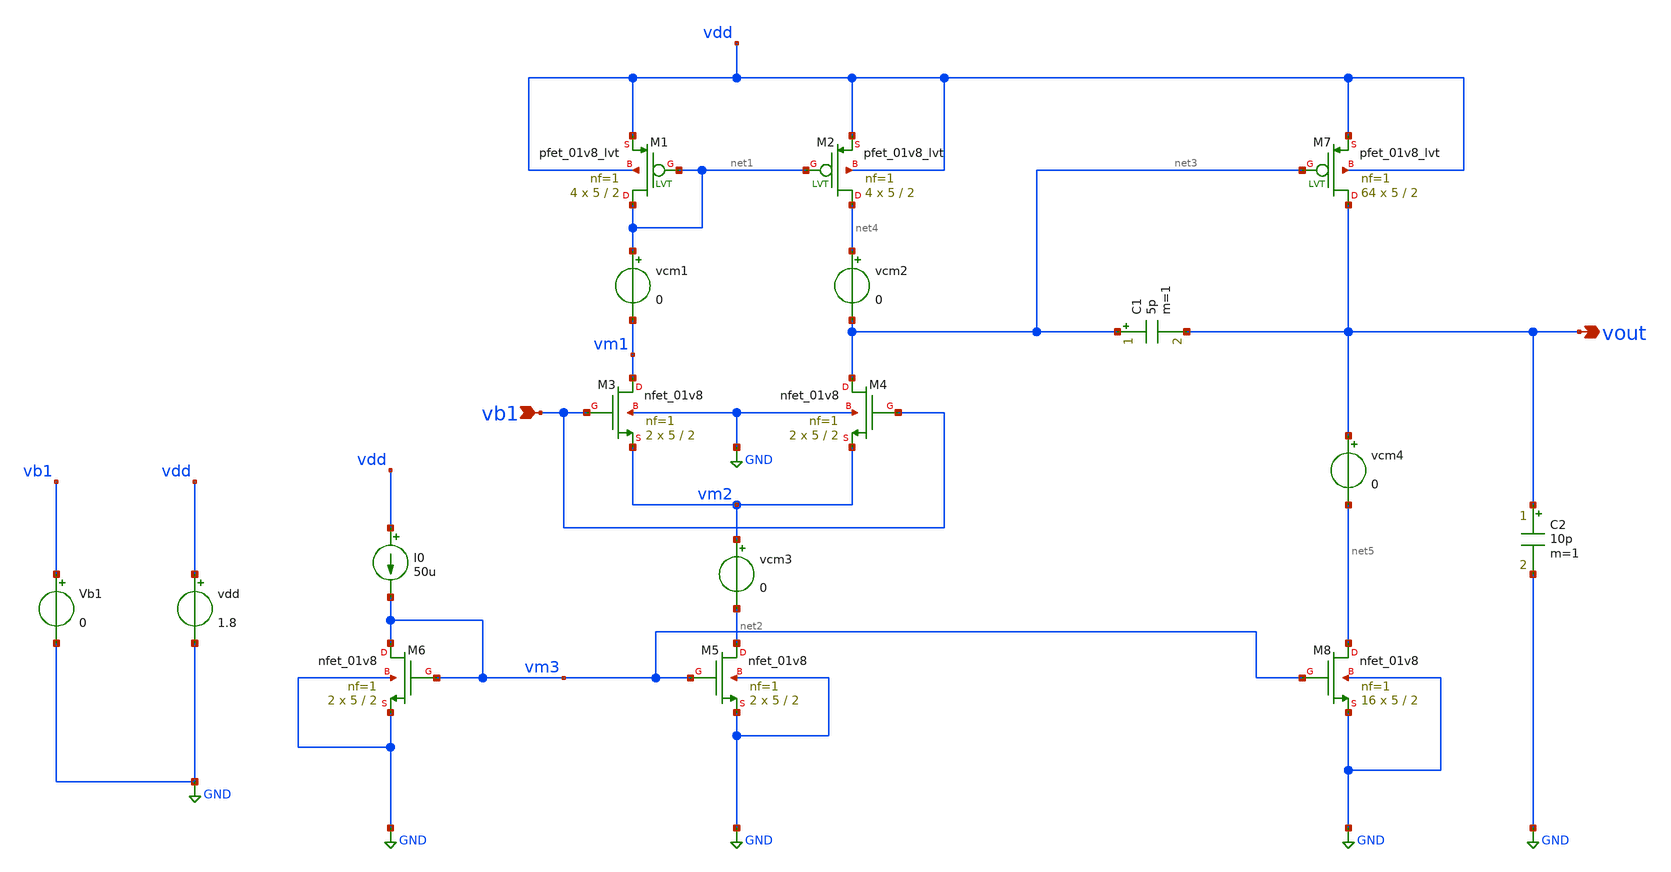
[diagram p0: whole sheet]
** sch_path: sch/Two_Stage_Differential_OpAMP.sch
**.subckt Two_Stage_Differential_OpAMP vb1 vout
*.ipin vb1
*.opin vout
XM5 net2 vm3 GND GND sky130_fd_pr__nfet_01v8 L=2 W=5 nf=1 ad='int((1 + 1)/2) * 5 / 1 * 0.29' as='int((1 + 2)/2) * 5 / 1 * 0.29'
+ pd='2*int((1 + 1)/2) * (5 / 1 + 0.29)' ps='2*int((1 + 2)/2) * (5 / 1 + 0.29)' nrd='0.29 / 5 ' nrs='0.29 / 5 '
+ sa=0 sb=0 sd=0 mult=2 m=2
I0 vdd vm3 50u
vdd vdd GND 1.8
Vb1 vb1 GND 0
XM2 net4 net1 vdd vdd sky130_fd_pr__pfet_01v8_lvt L=2 W=5 nf=1 ad='int((1 + 1)/2) * 5 / 1 * 0.29' as='int((1 + 2)/2) * 5 / 1 * 0.29'
+ pd='2*int((1 + 1)/2) * (5 / 1 + 0.29)' ps='2*int((1 + 2)/2) * (5 / 1 + 0.29)' nrd='0.29 / 5 ' nrs='0.29 / 5 '
+ sa=0 sb=0 sd=0 mult=4 m=4
XM3 vm1 vb1 vm2 GND sky130_fd_pr__nfet_01v8 L=2 W=5 nf=1 ad='int((1 + 1)/2) * 5 / 1 * 0.29' as='int((1 + 2)/2) * 5 / 1 * 0.29'
+ pd='2*int((1 + 1)/2) * (5 / 1 + 0.29)' ps='2*int((1 + 2)/2) * (5 / 1 + 0.29)' nrd='0.29 / 5 ' nrs='0.29 / 5 '
+ sa=0 sb=0 sd=0 mult=2 m=2
XM4 net3 vb1 vm2 GND sky130_fd_pr__nfet_01v8 L=2 W=5 nf=1 ad='int((1 + 1)/2) * 5 / 1 * 0.29' as='int((1 + 2)/2) * 5 / 1 * 0.29'
+ pd='2*int((1 + 1)/2) * (5 / 1 + 0.29)' ps='2*int((1 + 2)/2) * (5 / 1 + 0.29)' nrd='0.29 / 5 ' nrs='0.29 / 5 '
+ sa=0 sb=0 sd=0 mult=2 m=2
XM6 vm3 vm3 GND GND sky130_fd_pr__nfet_01v8 L=2 W=5 nf=1 ad='int((1 + 1)/2) * 5 / 1 * 0.29' as='int((1 + 2)/2) * 5 / 1 * 0.29'
+ pd='2*int((1 + 1)/2) * (5 / 1 + 0.29)' ps='2*int((1 + 2)/2) * (5 / 1 + 0.29)' nrd='0.29 / 5 ' nrs='0.29 / 5 '
+ sa=0 sb=0 sd=0 mult=2 m=2
XM1 net1 net1 vdd vdd sky130_fd_pr__pfet_01v8_lvt L=2 W=5 nf=1 ad='int((1 + 1)/2) * 5 / 1 * 0.29' as='int((1 + 2)/2) * 5 / 1 * 0.29'
+ pd='2*int((1 + 1)/2) * (5 / 1 + 0.29)' ps='2*int((1 + 2)/2) * (5 / 1 + 0.29)' nrd='0.29 / 5 ' nrs='0.29 / 5 '
+ sa=0 sb=0 sd=0 mult=4 m=4
vcm3 vm2 net2 0
vcm1 net1 vm1 0
vcm2 net4 net3 0
XM7 vout net3 vdd vdd sky130_fd_pr__pfet_01v8_lvt L=2 W=5 nf=1 ad='int((1 + 1)/2) * 5 / 1 * 0.29' as='int((1 + 2)/2) * 5 / 1 * 0.29'
+ pd='2*int((1 + 1)/2) * (5 / 1 + 0.29)' ps='2*int((1 + 2)/2) * (5 / 1 + 0.29)' nrd='0.29 / 5 ' nrs='0.29 / 5 '
+ sa=0 sb=0 sd=0 mult=64 m=64
XM8 net5 vm3 GND GND sky130_fd_pr__nfet_01v8 L=2 W=5 nf=1 ad='int((1 + 1)/2) * 5 / 1 * 0.29' as='int((1 + 2)/2) * 5 / 1 * 0.29'
+ pd='2*int((1 + 1)/2) * (5 / 1 + 0.29)' ps='2*int((1 + 2)/2) * (5 / 1 + 0.29)' nrd='0.29 / 5 ' nrs='0.29 / 5 '
+ sa=0 sb=0 sd=0 mult=16 m=16
C1 net3 vout 5p m=1
vcm4 vout net5 0
C2 vout GND 10p m=1
**** begin user architecture code

** opencircuitdesign pdks install
.lib $::SKYWATER_MODELS/sky130.lib.spice tt




* ngspice commands
.temp 27

.dc vb1 0 1.8 0.01


.control
run
save all

set color0 = white

plot i(vcm1)
plot i(vcm2)
plot i(vcm3)
plot i(vcm4)
plot i(vcm1) i(vcm2) i(vcm3) i(vcm4)

MEAS DC vtail FIND v(vm2) WHEN v(vb1)=1.1

*voltage measure
print v(vm1)[length(v(vm1))-1]
print v(vout)[length(v(vout))-1]
print v(vm2)[length(v(vm2))-1]
print v(vm3)[length(v(vm3))-1]

*plotting the vb1 vs the vm2
plot v(vb1) vs v(vm2)
plot v(vb1) v(vm1) v(vm2) v(vm3) v(vout)
plot v(vout)

.endc
.end



**** end user architecture code
**.ends
.GLOBAL GND
.end
